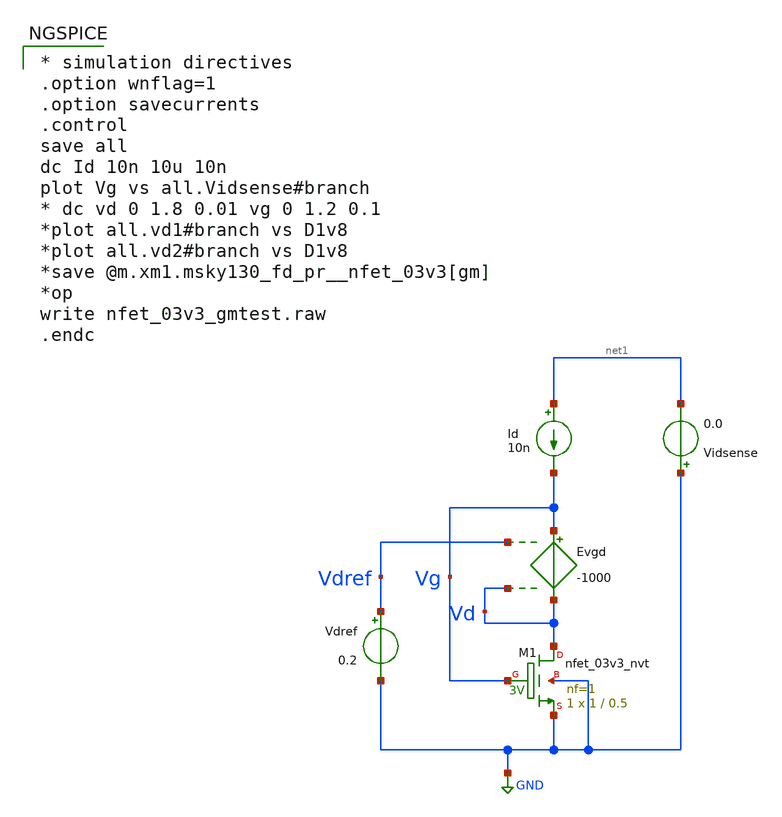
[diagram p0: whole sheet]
** sch_path: xschem/nfet_03v3_gmtest.sch
**.subckt nfet_03v3_gmtest
XM1 Vd Vg GND GND sky130_fd_pr__nfet_03v3_nvt L=0.5 W=1 nf=1 ad='int((nf+1)/2) * W/nf * 0.29' as='int((nf+2)/2) * W/nf * 0.29'
+ pd='2*int((nf+1)/2) * (W/nf + 0.29)' ps='2*int((nf+2)/2) * (W/nf + 0.29)' nrd='0.29 / W' nrs='0.29 / W'
+ sa=0 sb=0 sd=0 mult=1 m=1
Evgd Vg Vd Vdref Vd -1000
Id net1 Vg 10n
Vdref Vdref GND 0.2
Vidsense GND net1 0.0
**** begin user architecture code

** opencircuitdesign pdks install
.lib $::SKYWATER_MODELS/sky130.lib.spice tt



* simulation directives
.option wnflag=1
.option savecurrents
.control
save all
dc Id 10n 10u 10n
plot Vg vs all.Vidsense#branch
* dc vd 0 1.8 0.01 vg 0 1.2 0.1
*plot all.vd1#branch vs D1v8
*plot all.vd2#branch vs D1v8
*save @m.xm1.msky130_fd_pr__nfet_03v3[gm]
*op
write nfet_03v3_gmtest.raw
.endc


**** end user architecture code
**.ends
.GLOBAL GND
.end
